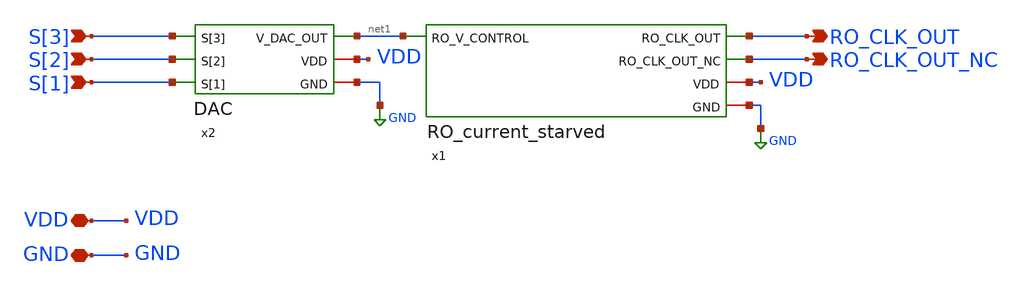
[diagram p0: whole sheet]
** sch_path: src/analog_source_files/RO_DAC.sch
**.subckt RO_DAC RO_CLK_OUT RO_CLK_OUT_NC S[3] S[2] S[1] VDD GND
*.opin RO_CLK_OUT
*.opin RO_CLK_OUT_NC
*.ipin S[3]
*.ipin S[2]
*.ipin S[1]
*.iopin VDD
*.iopin GND
x1 RO_CLK_OUT net1 VDD GND RO_CLK_OUT_NC RO_current_starved
x2 S[3] S[1] S[2] net1 VDD GND DAC
**.ends
.GLOBAL GND
.end
